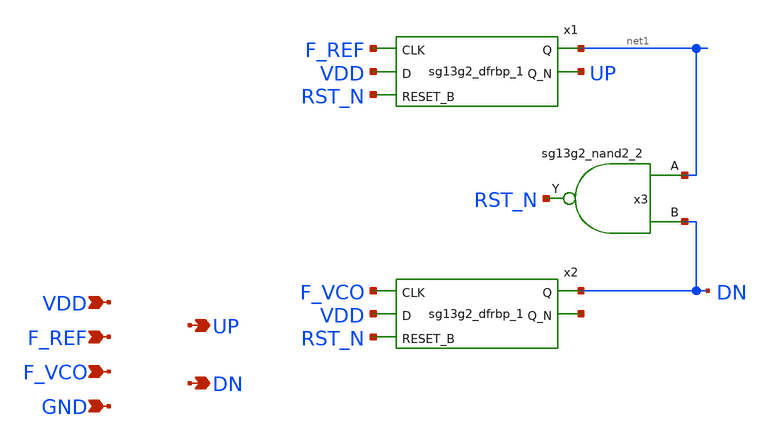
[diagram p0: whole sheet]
** sch_path: src/PFD_std.sch
**.subckt PFD_std UP F_REF VDD GND DN F_VCO
*.opin UP
*.ipin F_REF
*.ipin VDD
*.ipin GND
*.opin DN
*.ipin F_VCO
x1 net1 UP F_REF VDD RST_N VDD GND sg13g2_dfrbp_1
x2 DN net2 F_VCO VDD RST_N VDD GND sg13g2_dfrbp_1
x3 RST_N net1 DN VDD GND sg13g2_nand2_2
**.ends

* expanding   symbol:  sg13g2_stdcells/sg13g2_dfrbp_1.sym # of pins=5
** sym_path: sg13g2_stdcells/sg13g2_dfrbp_1.sym
** sch_path: sg13g2_stdcells/sg13g2_dfrbp_1.sch
.subckt sg13g2_dfrbp_1 Q Q_N CLK D RESET_B VDD VSS
*.ipin D
*.ipin RESET_B
*.ipin CLK
*.opin Q
*.opin Q_N
*.iopin VDD
*.iopin VSS
XM1 Db D net10 VSS sg13_lv_nmos w=420.00n l=130.00n ng=1 m=1 mm_ok=1
XM2 net10 RESET_B VSS VSS sg13_lv_nmos w=420.00n l=130.00n ng=1 m=1 mm_ok=1
XM3 net1 clkneg net9 VSS sg13_lv_nmos w=420.00n l=130.00n ng=1 m=1 mm_ok=1
XM4 net9 net1 VSS VSS sg13_lv_nmos w=420.00n l=130.00n ng=1 m=1 mm_ok=1
XM5 net1 net1 net5 VSS sg13_lv_nmos w=420.00n l=130.00n ng=1 m=1 mm_ok=1
XM6 net5 RESET_B VSS VSS sg13_lv_nmos w=420.00n l=130.00n ng=1 m=1 mm_ok=1
XM7 Q_N net1 VSS VSS sg13_lv_nmos w=740.00n l=130.00n ng=1 m=1 mm_ok=1
XM8 net2 net1 VSS VSS sg13_lv_nmos w=740.00n l=130.00n ng=1 m=1 mm_ok=1
XM9 Q net2 VSS VSS sg13_lv_nmos w=740.00n l=130.00n ng=1 m=1 mm_ok=1
XM10 clkneg CLK VSS VSS sg13_lv_nmos w=740.00n l=130.00n ng=1 m=1 mm_ok=1
XM11 clkpos clkneg VSS VSS sg13_lv_nmos w=740.00n l=130.00n ng=1 m=1 mm_ok=1
XM12 Db clkneg net3 VSS sg13_lv_nmos w=420.00n l=130.00n ng=1 m=1 mm_ok=1
XM13 net3 clkpos net8 VSS sg13_lv_nmos w=420.00n l=130.00n ng=1 m=1 mm_ok=1
XM14 net8 net3 net4 VSS sg13_lv_nmos w=420.00n l=130.00n ng=1 m=1 mm_ok=1
XM15 net4 RESET_B VSS VSS sg13_lv_nmos w=420.00n l=130.00n ng=1 m=1 mm_ok=1
XM16 net3 net3 VSS VSS sg13_lv_nmos w=740.00n l=130.00n ng=1 m=1 mm_ok=1
XM17 net3 clkpos net1 VSS sg13_lv_nmos w=740.00n l=130.00n ng=1 m=1 mm_ok=1
XM18 Db RESET_B VDD VDD sg13_lv_pmos w=420.00n l=130.00n ng=1 m=1 mm_ok=1
XM19 Db D VDD VDD sg13_lv_pmos w=420.00n l=130.00n ng=1 m=1 mm_ok=1
XM20 net7 net1 VDD VDD sg13_lv_pmos w=420.00n l=130.00n ng=1 m=1 mm_ok=1
XM21 net1 clkpos net7 VDD sg13_lv_pmos w=420.00n l=130.00n ng=1 m=1 mm_ok=1
XM22 net1 net1 VDD VDD sg13_lv_pmos w=420.00n l=130.00n ng=1 m=1 mm_ok=1
XM23 net1 RESET_B VDD VDD sg13_lv_pmos w=420.00n l=130.00n ng=1 m=1 mm_ok=1
XM24 Q_N net1 VDD VDD sg13_lv_pmos w=1.12u l=130.00n ng=1 m=1 mm_ok=1
XM25 net2 net1 VDD VDD sg13_lv_pmos w=1.12u l=130.00n ng=1 m=1 mm_ok=1
XM26 Q net2 VDD VDD sg13_lv_pmos w=1.12u l=130.00n ng=1 m=1 mm_ok=1
XM27 clkneg CLK VDD VDD sg13_lv_pmos w=1.12u l=130.00n ng=1 m=1 mm_ok=1
XM28 clkpos clkneg VDD VDD sg13_lv_pmos w=1.12u l=130.00n ng=1 m=1 mm_ok=1
XM29 Db clkpos net3 VDD sg13_lv_pmos w=420.00n l=130.00n ng=1 m=1 mm_ok=1
XM30 net6 net3 VDD VDD sg13_lv_pmos w=420.00n l=130.00n ng=1 m=1 mm_ok=1
XM31 net3 clkneg net6 VDD sg13_lv_pmos w=420.00n l=130.00n ng=1 m=1 mm_ok=1
XM32 net3 RESET_B VDD VDD sg13_lv_pmos w=420.00n l=130.00n ng=1 m=1 mm_ok=1
XM33 net3 net3 VDD VDD sg13_lv_pmos w=1.000u l=130.00n ng=1 m=1 mm_ok=1
XM34 net3 clkneg net1 VDD sg13_lv_pmos w=1.000u l=130.00n ng=1 m=1 mm_ok=1
.ends


* expanding   symbol:  sg13g2_stdcells/sg13g2_nand2_2.sym # of pins=3
** sym_path: sg13g2_stdcells/sg13g2_nand2_2.sym
** sch_path: sg13g2_stdcells/sg13g2_nand2_2.sch
.subckt sg13g2_nand2_2 Y A B VDD VSS
*.iopin VDD
*.iopin VSS
*.opin Y
*.ipin B
*.ipin A
XM1 Y A net1 VSS sg13_lv_nmos w=1.44u l=130.00n ng=2 m=1 mm_ok=1
XM2 net1 B VSS VSS sg13_lv_nmos w=1.44u l=130.00n ng=2 m=1 mm_ok=1
XM3 Y A VDD VDD sg13_lv_pmos w=2.24u l=130.00n ng=2 m=1 mm_ok=1
XM4 Y B VDD VDD sg13_lv_pmos w=2.24u l=130.00n ng=2 m=1 mm_ok=1
.ends

.end
